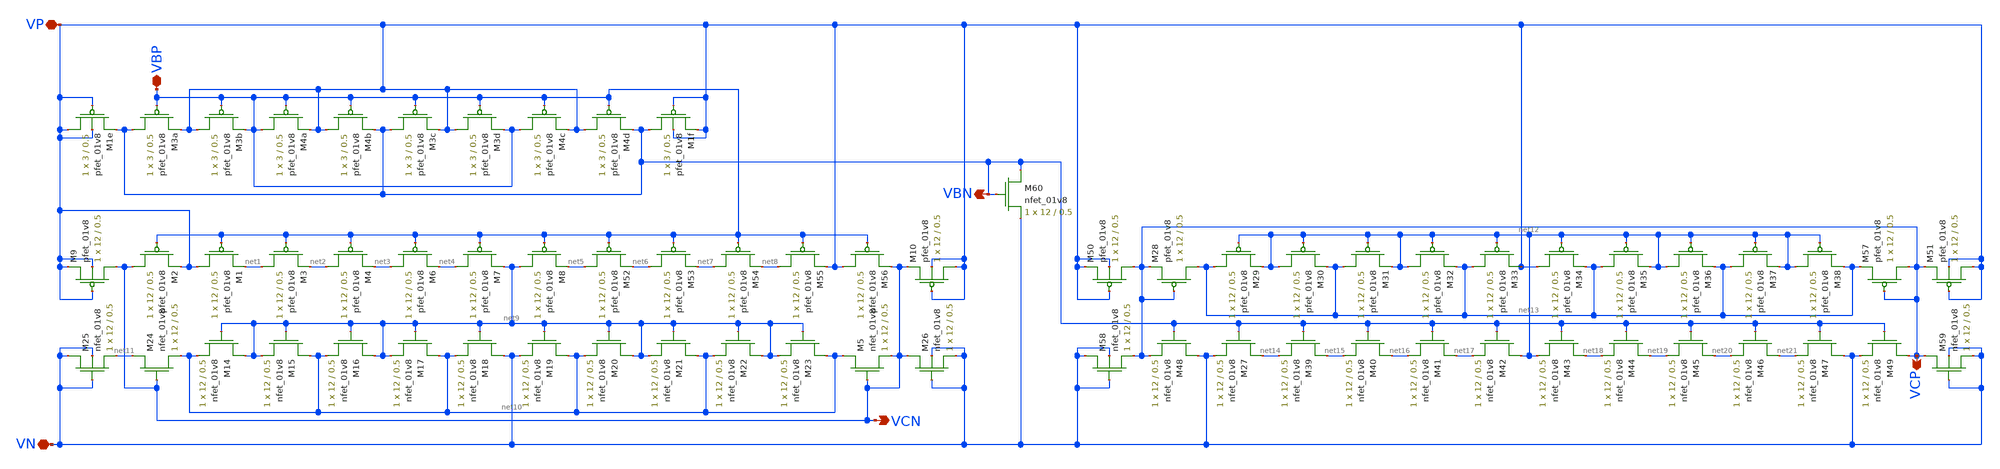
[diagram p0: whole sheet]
** sch_path: mp3/schematics/bias_generator_lds.sch
**.subckt bias_generator_lds VBP VP VN VCN VCP VBN
*.iopin VBP
*.iopin VP
*.iopin VN
*.opin VCN
*.opin VCP
*.opin VBN
XM9 VCN VP VP VP sky130_fd_pr__pfet_01v8 L=0.5 W=12 nf=1 ad='int((nf+1)/2) * W/nf * 0.29' as='int((nf+2)/2) * W/nf * 0.29'
+ pd='2*int((nf+1)/2) * (W/nf + 0.29)' ps='2*int((nf+2)/2) * (W/nf + 0.29)' nrd='0.29 / W' nrs='0.29 / W'
+ sa=0 sb=0 sd=0 mult=1 m=1
XM24 net11 VCN net10 GND sky130_fd_pr__nfet_01v8 L=0.5 W=12 nf=1 ad='int((nf+1)/2) * W/nf * 0.29' as='int((nf+2)/2) * W/nf * 0.29'
+ pd='2*int((nf+1)/2) * (W/nf + 0.29)' ps='2*int((nf+2)/2) * (W/nf + 0.29)' nrd='0.29 / W' nrs='0.29 / W'
+ sa=0 sb=0 sd=0 mult=1 m=1
XM2 VCN VBP VP VDD sky130_fd_pr__pfet_01v8 L=0.5 W=12 nf=1 ad='int((nf+1)/2) * W/nf * 0.29' as='int((nf+2)/2) * W/nf * 0.29'
+ pd='2*int((nf+1)/2) * (W/nf + 0.29)' ps='2*int((nf+2)/2) * (W/nf + 0.29)' nrd='0.29 / W' nrs='0.29 / W'
+ sa=0 sb=0 sd=0 mult=1 m=1
XM1 VP VBP net1 VDD sky130_fd_pr__pfet_01v8 L=0.5 W=12 nf=1 ad='int((nf+1)/2) * W/nf * 0.29' as='int((nf+2)/2) * W/nf * 0.29'
+ pd='2*int((nf+1)/2) * (W/nf + 0.29)' ps='2*int((nf+2)/2) * (W/nf + 0.29)' nrd='0.29 / W' nrs='0.29 / W'
+ sa=0 sb=0 sd=0 mult=1 m=1
XM3 net1 VBP net2 VDD sky130_fd_pr__pfet_01v8 L=0.5 W=12 nf=1 ad='int((nf+1)/2) * W/nf * 0.29' as='int((nf+2)/2) * W/nf * 0.29'
+ pd='2*int((nf+1)/2) * (W/nf + 0.29)' ps='2*int((nf+2)/2) * (W/nf + 0.29)' nrd='0.29 / W' nrs='0.29 / W'
+ sa=0 sb=0 sd=0 mult=1 m=1
XM4 net2 VBP net3 VDD sky130_fd_pr__pfet_01v8 L=0.5 W=12 nf=1 ad='int((nf+1)/2) * W/nf * 0.29' as='int((nf+2)/2) * W/nf * 0.29'
+ pd='2*int((nf+1)/2) * (W/nf + 0.29)' ps='2*int((nf+2)/2) * (W/nf + 0.29)' nrd='0.29 / W' nrs='0.29 / W'
+ sa=0 sb=0 sd=0 mult=1 m=1
XM6 net3 VBP net4 VDD sky130_fd_pr__pfet_01v8 L=0.5 W=12 nf=1 ad='int((nf+1)/2) * W/nf * 0.29' as='int((nf+2)/2) * W/nf * 0.29'
+ pd='2*int((nf+1)/2) * (W/nf + 0.29)' ps='2*int((nf+2)/2) * (W/nf + 0.29)' nrd='0.29 / W' nrs='0.29 / W'
+ sa=0 sb=0 sd=0 mult=1 m=1
XM7 net4 VBP net9 VDD sky130_fd_pr__pfet_01v8 L=0.5 W=12 nf=1 ad='int((nf+1)/2) * W/nf * 0.29' as='int((nf+2)/2) * W/nf * 0.29'
+ pd='2*int((nf+1)/2) * (W/nf + 0.29)' ps='2*int((nf+2)/2) * (W/nf + 0.29)' nrd='0.29 / W' nrs='0.29 / W'
+ sa=0 sb=0 sd=0 mult=1 m=1
XM8 net9 VBP net5 VDD sky130_fd_pr__pfet_01v8 L=0.5 W=12 nf=1 ad='int((nf+1)/2) * W/nf * 0.29' as='int((nf+2)/2) * W/nf * 0.29'
+ pd='2*int((nf+1)/2) * (W/nf + 0.29)' ps='2*int((nf+2)/2) * (W/nf + 0.29)' nrd='0.29 / W' nrs='0.29 / W'
+ sa=0 sb=0 sd=0 mult=1 m=1
XM52 net5 VBP net6 VDD sky130_fd_pr__pfet_01v8 L=0.5 W=12 nf=1 ad='int((nf+1)/2) * W/nf * 0.29' as='int((nf+2)/2) * W/nf * 0.29'
+ pd='2*int((nf+1)/2) * (W/nf + 0.29)' ps='2*int((nf+2)/2) * (W/nf + 0.29)' nrd='0.29 / W' nrs='0.29 / W'
+ sa=0 sb=0 sd=0 mult=1 m=1
XM53 net6 VBP net7 VDD sky130_fd_pr__pfet_01v8 L=0.5 W=12 nf=1 ad='int((nf+1)/2) * W/nf * 0.29' as='int((nf+2)/2) * W/nf * 0.29'
+ pd='2*int((nf+1)/2) * (W/nf + 0.29)' ps='2*int((nf+2)/2) * (W/nf + 0.29)' nrd='0.29 / W' nrs='0.29 / W'
+ sa=0 sb=0 sd=0 mult=1 m=1
XM54 net7 VBP net8 VDD sky130_fd_pr__pfet_01v8 L=0.5 W=12 nf=1 ad='int((nf+1)/2) * W/nf * 0.29' as='int((nf+2)/2) * W/nf * 0.29'
+ pd='2*int((nf+1)/2) * (W/nf + 0.29)' ps='2*int((nf+2)/2) * (W/nf + 0.29)' nrd='0.29 / W' nrs='0.29 / W'
+ sa=0 sb=0 sd=0 mult=1 m=1
XM55 net8 VBP VP VDD sky130_fd_pr__pfet_01v8 L=0.5 W=12 nf=1 ad='int((nf+1)/2) * W/nf * 0.29' as='int((nf+2)/2) * W/nf * 0.29'
+ pd='2*int((nf+1)/2) * (W/nf + 0.29)' ps='2*int((nf+2)/2) * (W/nf + 0.29)' nrd='0.29 / W' nrs='0.29 / W'
+ sa=0 sb=0 sd=0 mult=1 m=1
XM56 VP VBP VCN VDD sky130_fd_pr__pfet_01v8 L=0.5 W=12 nf=1 ad='int((nf+1)/2) * W/nf * 0.29' as='int((nf+2)/2) * W/nf * 0.29'
+ pd='2*int((nf+1)/2) * (W/nf + 0.29)' ps='2*int((nf+2)/2) * (W/nf + 0.29)' nrd='0.29 / W' nrs='0.29 / W'
+ sa=0 sb=0 sd=0 mult=1 m=1
XM10 VP VP VCN VP sky130_fd_pr__pfet_01v8 L=0.5 W=12 nf=1 ad='int((nf+1)/2) * W/nf * 0.29' as='int((nf+2)/2) * W/nf * 0.29'
+ pd='2*int((nf+1)/2) * (W/nf + 0.29)' ps='2*int((nf+2)/2) * (W/nf + 0.29)' nrd='0.29 / W' nrs='0.29 / W'
+ sa=0 sb=0 sd=0 mult=1 m=1
XM25 VN VN net11 VN sky130_fd_pr__nfet_01v8 L=0.5 W=12 nf=1 ad='int((nf+1)/2) * W/nf * 0.29' as='int((nf+2)/2) * W/nf * 0.29'
+ pd='2*int((nf+1)/2) * (W/nf + 0.29)' ps='2*int((nf+2)/2) * (W/nf + 0.29)' nrd='0.29 / W' nrs='0.29 / W'
+ sa=0 sb=0 sd=0 mult=1 m=1
XM14 net9 net9 net10 GND sky130_fd_pr__nfet_01v8 L=0.5 W=12 nf=1 ad='int((nf+1)/2) * W/nf * 0.29' as='int((nf+2)/2) * W/nf * 0.29'
+ pd='2*int((nf+1)/2) * (W/nf + 0.29)' ps='2*int((nf+2)/2) * (W/nf + 0.29)' nrd='0.29 / W' nrs='0.29 / W'
+ sa=0 sb=0 sd=0 mult=1 m=1
XM15 net10 net9 net9 GND sky130_fd_pr__nfet_01v8 L=0.5 W=12 nf=1 ad='int((nf+1)/2) * W/nf * 0.29' as='int((nf+2)/2) * W/nf * 0.29'
+ pd='2*int((nf+1)/2) * (W/nf + 0.29)' ps='2*int((nf+2)/2) * (W/nf + 0.29)' nrd='0.29 / W' nrs='0.29 / W'
+ sa=0 sb=0 sd=0 mult=1 m=1
XM16 net9 net9 net10 GND sky130_fd_pr__nfet_01v8 L=0.5 W=12 nf=1 ad='int((nf+1)/2) * W/nf * 0.29' as='int((nf+2)/2) * W/nf * 0.29'
+ pd='2*int((nf+1)/2) * (W/nf + 0.29)' ps='2*int((nf+2)/2) * (W/nf + 0.29)' nrd='0.29 / W' nrs='0.29 / W'
+ sa=0 sb=0 sd=0 mult=1 m=1
XM17 net10 net9 net9 GND sky130_fd_pr__nfet_01v8 L=0.5 W=12 nf=1 ad='int((nf+1)/2) * W/nf * 0.29' as='int((nf+2)/2) * W/nf * 0.29'
+ pd='2*int((nf+1)/2) * (W/nf + 0.29)' ps='2*int((nf+2)/2) * (W/nf + 0.29)' nrd='0.29 / W' nrs='0.29 / W'
+ sa=0 sb=0 sd=0 mult=1 m=1
XM18 VN net9 net10 GND sky130_fd_pr__nfet_01v8 L=0.5 W=12 nf=1 ad='int((nf+1)/2) * W/nf * 0.29' as='int((nf+2)/2) * W/nf * 0.29'
+ pd='2*int((nf+1)/2) * (W/nf + 0.29)' ps='2*int((nf+2)/2) * (W/nf + 0.29)' nrd='0.29 / W' nrs='0.29 / W'
+ sa=0 sb=0 sd=0 mult=1 m=1
XM19 net10 net9 VN GND sky130_fd_pr__nfet_01v8 L=0.5 W=12 nf=1 ad='int((nf+1)/2) * W/nf * 0.29' as='int((nf+2)/2) * W/nf * 0.29'
+ pd='2*int((nf+1)/2) * (W/nf + 0.29)' ps='2*int((nf+2)/2) * (W/nf + 0.29)' nrd='0.29 / W' nrs='0.29 / W'
+ sa=0 sb=0 sd=0 mult=1 m=1
XM20 net9 net9 net10 GND sky130_fd_pr__nfet_01v8 L=0.5 W=12 nf=1 ad='int((nf+1)/2) * W/nf * 0.29' as='int((nf+2)/2) * W/nf * 0.29'
+ pd='2*int((nf+1)/2) * (W/nf + 0.29)' ps='2*int((nf+2)/2) * (W/nf + 0.29)' nrd='0.29 / W' nrs='0.29 / W'
+ sa=0 sb=0 sd=0 mult=1 m=1
XM21 net10 net9 net9 GND sky130_fd_pr__nfet_01v8 L=0.5 W=12 nf=1 ad='int((nf+1)/2) * W/nf * 0.29' as='int((nf+2)/2) * W/nf * 0.29'
+ pd='2*int((nf+1)/2) * (W/nf + 0.29)' ps='2*int((nf+2)/2) * (W/nf + 0.29)' nrd='0.29 / W' nrs='0.29 / W'
+ sa=0 sb=0 sd=0 mult=1 m=1
XM22 net9 net9 net10 GND sky130_fd_pr__nfet_01v8 L=0.5 W=12 nf=1 ad='int((nf+1)/2) * W/nf * 0.29' as='int((nf+2)/2) * W/nf * 0.29'
+ pd='2*int((nf+1)/2) * (W/nf + 0.29)' ps='2*int((nf+2)/2) * (W/nf + 0.29)' nrd='0.29 / W' nrs='0.29 / W'
+ sa=0 sb=0 sd=0 mult=1 m=1
XM23 net10 net9 net9 GND sky130_fd_pr__nfet_01v8 L=0.5 W=12 nf=1 ad='int((nf+1)/2) * W/nf * 0.29' as='int((nf+2)/2) * W/nf * 0.29'
+ pd='2*int((nf+1)/2) * (W/nf + 0.29)' ps='2*int((nf+2)/2) * (W/nf + 0.29)' nrd='0.29 / W' nrs='0.29 / W'
+ sa=0 sb=0 sd=0 mult=1 m=1
XM5 net10 VCN VCN GND sky130_fd_pr__nfet_01v8 L=0.5 W=12 nf=1 ad='int((nf+1)/2) * W/nf * 0.29' as='int((nf+2)/2) * W/nf * 0.29'
+ pd='2*int((nf+1)/2) * (W/nf + 0.29)' ps='2*int((nf+2)/2) * (W/nf + 0.29)' nrd='0.29 / W' nrs='0.29 / W'
+ sa=0 sb=0 sd=0 mult=1 m=1
XM26 VCN VN VN VN sky130_fd_pr__nfet_01v8 L=0.5 W=12 nf=1 ad='int((nf+1)/2) * W/nf * 0.29' as='int((nf+2)/2) * W/nf * 0.29'
+ pd='2*int((nf+1)/2) * (W/nf + 0.29)' ps='2*int((nf+2)/2) * (W/nf + 0.29)' nrd='0.29 / W' nrs='0.29 / W'
+ sa=0 sb=0 sd=0 mult=1 m=1
XM27 net14 VBN VN GND sky130_fd_pr__nfet_01v8 L=0.5 W=12 nf=1 ad='int((nf+1)/2) * W/nf * 0.29' as='int((nf+2)/2) * W/nf * 0.29'
+ pd='2*int((nf+1)/2) * (W/nf + 0.29)' ps='2*int((nf+2)/2) * (W/nf + 0.29)' nrd='0.29 / W' nrs='0.29 / W'
+ sa=0 sb=0 sd=0 mult=1 m=1
XM39 net15 VBN net14 GND sky130_fd_pr__nfet_01v8 L=0.5 W=12 nf=1 ad='int((nf+1)/2) * W/nf * 0.29' as='int((nf+2)/2) * W/nf * 0.29'
+ pd='2*int((nf+1)/2) * (W/nf + 0.29)' ps='2*int((nf+2)/2) * (W/nf + 0.29)' nrd='0.29 / W' nrs='0.29 / W'
+ sa=0 sb=0 sd=0 mult=1 m=1
XM40 net16 VBN net15 GND sky130_fd_pr__nfet_01v8 L=0.5 W=12 nf=1 ad='int((nf+1)/2) * W/nf * 0.29' as='int((nf+2)/2) * W/nf * 0.29'
+ pd='2*int((nf+1)/2) * (W/nf + 0.29)' ps='2*int((nf+2)/2) * (W/nf + 0.29)' nrd='0.29 / W' nrs='0.29 / W'
+ sa=0 sb=0 sd=0 mult=1 m=1
XM41 net17 VBN net16 GND sky130_fd_pr__nfet_01v8 L=0.5 W=12 nf=1 ad='int((nf+1)/2) * W/nf * 0.29' as='int((nf+2)/2) * W/nf * 0.29'
+ pd='2*int((nf+1)/2) * (W/nf + 0.29)' ps='2*int((nf+2)/2) * (W/nf + 0.29)' nrd='0.29 / W' nrs='0.29 / W'
+ sa=0 sb=0 sd=0 mult=1 m=1
XM42 net12 VBN net17 GND sky130_fd_pr__nfet_01v8 L=0.5 W=12 nf=1 ad='int((nf+1)/2) * W/nf * 0.29' as='int((nf+2)/2) * W/nf * 0.29'
+ pd='2*int((nf+1)/2) * (W/nf + 0.29)' ps='2*int((nf+2)/2) * (W/nf + 0.29)' nrd='0.29 / W' nrs='0.29 / W'
+ sa=0 sb=0 sd=0 mult=1 m=1
XM43 net18 VBN net12 GND sky130_fd_pr__nfet_01v8 L=0.5 W=12 nf=1 ad='int((nf+1)/2) * W/nf * 0.29' as='int((nf+2)/2) * W/nf * 0.29'
+ pd='2*int((nf+1)/2) * (W/nf + 0.29)' ps='2*int((nf+2)/2) * (W/nf + 0.29)' nrd='0.29 / W' nrs='0.29 / W'
+ sa=0 sb=0 sd=0 mult=1 m=1
XM44 net19 VBN net18 GND sky130_fd_pr__nfet_01v8 L=0.5 W=12 nf=1 ad='int((nf+1)/2) * W/nf * 0.29' as='int((nf+2)/2) * W/nf * 0.29'
+ pd='2*int((nf+1)/2) * (W/nf + 0.29)' ps='2*int((nf+2)/2) * (W/nf + 0.29)' nrd='0.29 / W' nrs='0.29 / W'
+ sa=0 sb=0 sd=0 mult=1 m=1
XM45 net20 VBN net19 GND sky130_fd_pr__nfet_01v8 L=0.5 W=12 nf=1 ad='int((nf+1)/2) * W/nf * 0.29' as='int((nf+2)/2) * W/nf * 0.29'
+ pd='2*int((nf+1)/2) * (W/nf + 0.29)' ps='2*int((nf+2)/2) * (W/nf + 0.29)' nrd='0.29 / W' nrs='0.29 / W'
+ sa=0 sb=0 sd=0 mult=1 m=1
XM46 net21 VBN net20 GND sky130_fd_pr__nfet_01v8 L=0.5 W=12 nf=1 ad='int((nf+1)/2) * W/nf * 0.29' as='int((nf+2)/2) * W/nf * 0.29'
+ pd='2*int((nf+1)/2) * (W/nf + 0.29)' ps='2*int((nf+2)/2) * (W/nf + 0.29)' nrd='0.29 / W' nrs='0.29 / W'
+ sa=0 sb=0 sd=0 mult=1 m=1
XM47 VN VBN net21 GND sky130_fd_pr__nfet_01v8 L=0.5 W=12 nf=1 ad='int((nf+1)/2) * W/nf * 0.29' as='int((nf+2)/2) * W/nf * 0.29'
+ pd='2*int((nf+1)/2) * (W/nf + 0.29)' ps='2*int((nf+2)/2) * (W/nf + 0.29)' nrd='0.29 / W' nrs='0.29 / W'
+ sa=0 sb=0 sd=0 mult=1 m=1
XM48 VN VBN VCP GND sky130_fd_pr__nfet_01v8 L=0.5 W=12 nf=1 ad='int((nf+1)/2) * W/nf * 0.29' as='int((nf+2)/2) * W/nf * 0.29'
+ pd='2*int((nf+1)/2) * (W/nf + 0.29)' ps='2*int((nf+2)/2) * (W/nf + 0.29)' nrd='0.29 / W' nrs='0.29 / W'
+ sa=0 sb=0 sd=0 mult=1 m=1
XM49 VCP VBN VN GND sky130_fd_pr__nfet_01v8 L=0.5 W=12 nf=1 ad='int((nf+1)/2) * W/nf * 0.29' as='int((nf+2)/2) * W/nf * 0.29'
+ pd='2*int((nf+1)/2) * (W/nf + 0.29)' ps='2*int((nf+2)/2) * (W/nf + 0.29)' nrd='0.29 / W' nrs='0.29 / W'
+ sa=0 sb=0 sd=0 mult=1 m=1
XM29 net13 net12 net12 VDD sky130_fd_pr__pfet_01v8 L=0.5 W=12 nf=1 ad='int((nf+1)/2) * W/nf * 0.29' as='int((nf+2)/2) * W/nf * 0.29'
+ pd='2*int((nf+1)/2) * (W/nf + 0.29)' ps='2*int((nf+2)/2) * (W/nf + 0.29)' nrd='0.29 / W' nrs='0.29 / W'
+ sa=0 sb=0 sd=0 mult=1 m=1
XM30 net12 net12 net13 VDD sky130_fd_pr__pfet_01v8 L=0.5 W=12 nf=1 ad='int((nf+1)/2) * W/nf * 0.29' as='int((nf+2)/2) * W/nf * 0.29'
+ pd='2*int((nf+1)/2) * (W/nf + 0.29)' ps='2*int((nf+2)/2) * (W/nf + 0.29)' nrd='0.29 / W' nrs='0.29 / W'
+ sa=0 sb=0 sd=0 mult=1 m=1
XM31 net13 net12 net12 VDD sky130_fd_pr__pfet_01v8 L=0.5 W=12 nf=1 ad='int((nf+1)/2) * W/nf * 0.29' as='int((nf+2)/2) * W/nf * 0.29'
+ pd='2*int((nf+1)/2) * (W/nf + 0.29)' ps='2*int((nf+2)/2) * (W/nf + 0.29)' nrd='0.29 / W' nrs='0.29 / W'
+ sa=0 sb=0 sd=0 mult=1 m=1
XM32 net12 net12 net13 VDD sky130_fd_pr__pfet_01v8 L=0.5 W=12 nf=1 ad='int((nf+1)/2) * W/nf * 0.29' as='int((nf+2)/2) * W/nf * 0.29'
+ pd='2*int((nf+1)/2) * (W/nf + 0.29)' ps='2*int((nf+2)/2) * (W/nf + 0.29)' nrd='0.29 / W' nrs='0.29 / W'
+ sa=0 sb=0 sd=0 mult=1 m=1
XM33 net13 net12 VP VDD sky130_fd_pr__pfet_01v8 L=0.5 W=12 nf=1 ad='int((nf+1)/2) * W/nf * 0.29' as='int((nf+2)/2) * W/nf * 0.29'
+ pd='2*int((nf+1)/2) * (W/nf + 0.29)' ps='2*int((nf+2)/2) * (W/nf + 0.29)' nrd='0.29 / W' nrs='0.29 / W'
+ sa=0 sb=0 sd=0 mult=1 m=1
XM34 VP net12 net13 VDD sky130_fd_pr__pfet_01v8 L=0.5 W=12 nf=1 ad='int((nf+1)/2) * W/nf * 0.29' as='int((nf+2)/2) * W/nf * 0.29'
+ pd='2*int((nf+1)/2) * (W/nf + 0.29)' ps='2*int((nf+2)/2) * (W/nf + 0.29)' nrd='0.29 / W' nrs='0.29 / W'
+ sa=0 sb=0 sd=0 mult=1 m=1
XM35 net13 net12 net12 VDD sky130_fd_pr__pfet_01v8 L=0.5 W=12 nf=1 ad='int((nf+1)/2) * W/nf * 0.29' as='int((nf+2)/2) * W/nf * 0.29'
+ pd='2*int((nf+1)/2) * (W/nf + 0.29)' ps='2*int((nf+2)/2) * (W/nf + 0.29)' nrd='0.29 / W' nrs='0.29 / W'
+ sa=0 sb=0 sd=0 mult=1 m=1
XM36 net12 net12 net13 VDD sky130_fd_pr__pfet_01v8 L=0.5 W=12 nf=1 ad='int((nf+1)/2) * W/nf * 0.29' as='int((nf+2)/2) * W/nf * 0.29'
+ pd='2*int((nf+1)/2) * (W/nf + 0.29)' ps='2*int((nf+2)/2) * (W/nf + 0.29)' nrd='0.29 / W' nrs='0.29 / W'
+ sa=0 sb=0 sd=0 mult=1 m=1
XM37 net13 net12 net12 VDD sky130_fd_pr__pfet_01v8 L=0.5 W=12 nf=1 ad='int((nf+1)/2) * W/nf * 0.29' as='int((nf+2)/2) * W/nf * 0.29'
+ pd='2*int((nf+1)/2) * (W/nf + 0.29)' ps='2*int((nf+2)/2) * (W/nf + 0.29)' nrd='0.29 / W' nrs='0.29 / W'
+ sa=0 sb=0 sd=0 mult=1 m=1
XM38 net12 net12 net13 VDD sky130_fd_pr__pfet_01v8 L=0.5 W=12 nf=1 ad='int((nf+1)/2) * W/nf * 0.29' as='int((nf+2)/2) * W/nf * 0.29'
+ pd='2*int((nf+1)/2) * (W/nf + 0.29)' ps='2*int((nf+2)/2) * (W/nf + 0.29)' nrd='0.29 / W' nrs='0.29 / W'
+ sa=0 sb=0 sd=0 mult=1 m=1
XM57 VCP VCP net13 VDD sky130_fd_pr__pfet_01v8 L=0.5 W=12 nf=1 ad='int((nf+1)/2) * W/nf * 0.29' as='int((nf+2)/2) * W/nf * 0.29'
+ pd='2*int((nf+1)/2) * (W/nf + 0.29)' ps='2*int((nf+2)/2) * (W/nf + 0.29)' nrd='0.29 / W' nrs='0.29 / W'
+ sa=0 sb=0 sd=0 mult=1 m=1
XM28 net13 VCP VCP VDD sky130_fd_pr__pfet_01v8 L=0.5 W=12 nf=1 ad='int((nf+1)/2) * W/nf * 0.29' as='int((nf+2)/2) * W/nf * 0.29'
+ pd='2*int((nf+1)/2) * (W/nf + 0.29)' ps='2*int((nf+2)/2) * (W/nf + 0.29)' nrd='0.29 / W' nrs='0.29 / W'
+ sa=0 sb=0 sd=0 mult=1 m=1
XM50 VCP VP VP VP sky130_fd_pr__pfet_01v8 L=0.5 W=12 nf=1 ad='int((nf+1)/2) * W/nf * 0.29' as='int((nf+2)/2) * W/nf * 0.29'
+ pd='2*int((nf+1)/2) * (W/nf + 0.29)' ps='2*int((nf+2)/2) * (W/nf + 0.29)' nrd='0.29 / W' nrs='0.29 / W'
+ sa=0 sb=0 sd=0 mult=1 m=1
XM51 VP VP VCP VP sky130_fd_pr__pfet_01v8 L=0.5 W=12 nf=1 ad='int((nf+1)/2) * W/nf * 0.29' as='int((nf+2)/2) * W/nf * 0.29'
+ pd='2*int((nf+1)/2) * (W/nf + 0.29)' ps='2*int((nf+2)/2) * (W/nf + 0.29)' nrd='0.29 / W' nrs='0.29 / W'
+ sa=0 sb=0 sd=0 mult=1 m=1
XM58 VN VN VCP VN sky130_fd_pr__nfet_01v8 L=0.5 W=12 nf=1 ad='int((nf+1)/2) * W/nf * 0.29' as='int((nf+2)/2) * W/nf * 0.29'
+ pd='2*int((nf+1)/2) * (W/nf + 0.29)' ps='2*int((nf+2)/2) * (W/nf + 0.29)' nrd='0.29 / W' nrs='0.29 / W'
+ sa=0 sb=0 sd=0 mult=1 m=1
XM59 VCP VN VN VN sky130_fd_pr__nfet_01v8 L=0.5 W=12 nf=1 ad='int((nf+1)/2) * W/nf * 0.29' as='int((nf+2)/2) * W/nf * 0.29'
+ pd='2*int((nf+1)/2) * (W/nf + 0.29)' ps='2*int((nf+2)/2) * (W/nf + 0.29)' nrd='0.29 / W' nrs='0.29 / W'
+ sa=0 sb=0 sd=0 mult=1 m=1
XM3b VP VBP VBP VDD sky130_fd_pr__pfet_01v8 L=0.5 W=3 nf=1 ad='int((nf+1)/2) * W/nf * 0.29' as='int((nf+2)/2) * W/nf * 0.29'
+ pd='2*int((nf+1)/2) * (W/nf + 0.29)' ps='2*int((nf+2)/2) * (W/nf + 0.29)' nrd='0.29 / W' nrs='0.29 / W'
+ sa=0 sb=0 sd=0 mult=1 m=1
XM3a VBN VBP VP VDD sky130_fd_pr__pfet_01v8 L=0.5 W=3 nf=1 ad='int((nf+1)/2) * W/nf * 0.29' as='int((nf+2)/2) * W/nf * 0.29'
+ pd='2*int((nf+1)/2) * (W/nf + 0.29)' ps='2*int((nf+2)/2) * (W/nf + 0.29)' nrd='0.29 / W' nrs='0.29 / W'
+ sa=0 sb=0 sd=0 mult=1 m=1
XM4a VBP VBP VP VDD sky130_fd_pr__pfet_01v8 L=0.5 W=3 nf=1 ad='int((nf+1)/2) * W/nf * 0.29' as='int((nf+2)/2) * W/nf * 0.29'
+ pd='2*int((nf+1)/2) * (W/nf + 0.29)' ps='2*int((nf+2)/2) * (W/nf + 0.29)' nrd='0.29 / W' nrs='0.29 / W'
+ sa=0 sb=0 sd=0 mult=1 m=1
XM4b VP VBP VBN VDD sky130_fd_pr__pfet_01v8 L=0.5 W=3 nf=1 ad='int((nf+1)/2) * W/nf * 0.29' as='int((nf+2)/2) * W/nf * 0.29'
+ pd='2*int((nf+1)/2) * (W/nf + 0.29)' ps='2*int((nf+2)/2) * (W/nf + 0.29)' nrd='0.29 / W' nrs='0.29 / W'
+ sa=0 sb=0 sd=0 mult=1 m=1
XM3c VBN VBP VP VDD sky130_fd_pr__pfet_01v8 L=0.5 W=3 nf=1 ad='int((nf+1)/2) * W/nf * 0.29' as='int((nf+2)/2) * W/nf * 0.29'
+ pd='2*int((nf+1)/2) * (W/nf + 0.29)' ps='2*int((nf+2)/2) * (W/nf + 0.29)' nrd='0.29 / W' nrs='0.29 / W'
+ sa=0 sb=0 sd=0 mult=1 m=1
XM3d VP VBP VBP VDD sky130_fd_pr__pfet_01v8 L=0.5 W=3 nf=1 ad='int((nf+1)/2) * W/nf * 0.29' as='int((nf+2)/2) * W/nf * 0.29'
+ pd='2*int((nf+1)/2) * (W/nf + 0.29)' ps='2*int((nf+2)/2) * (W/nf + 0.29)' nrd='0.29 / W' nrs='0.29 / W'
+ sa=0 sb=0 sd=0 mult=1 m=1
XM4c VBP VBP VP VDD sky130_fd_pr__pfet_01v8 L=0.5 W=3 nf=1 ad='int((nf+1)/2) * W/nf * 0.29' as='int((nf+2)/2) * W/nf * 0.29'
+ pd='2*int((nf+1)/2) * (W/nf + 0.29)' ps='2*int((nf+2)/2) * (W/nf + 0.29)' nrd='0.29 / W' nrs='0.29 / W'
+ sa=0 sb=0 sd=0 mult=1 m=1
XM1e VP VP VBN VP sky130_fd_pr__pfet_01v8 L=0.5 W=3 nf=1 ad='int((nf+1)/2) * W/nf * 0.29' as='int((nf+2)/2) * W/nf * 0.29'
+ pd='2*int((nf+1)/2) * (W/nf + 0.29)' ps='2*int((nf+2)/2) * (W/nf + 0.29)' nrd='0.29 / W' nrs='0.29 / W'
+ sa=0 sb=0 sd=0 mult=1 m=1
XM1f VBN VP VP VP sky130_fd_pr__pfet_01v8 L=0.5 W=3 nf=1 ad='int((nf+1)/2) * W/nf * 0.29' as='int((nf+2)/2) * W/nf * 0.29'
+ pd='2*int((nf+1)/2) * (W/nf + 0.29)' ps='2*int((nf+2)/2) * (W/nf + 0.29)' nrd='0.29 / W' nrs='0.29 / W'
+ sa=0 sb=0 sd=0 mult=1 m=1
XM4d VP VBP VBN VDD sky130_fd_pr__pfet_01v8 L=0.5 W=3 nf=1 ad='int((nf+1)/2) * W/nf * 0.29' as='int((nf+2)/2) * W/nf * 0.29'
+ pd='2*int((nf+1)/2) * (W/nf + 0.29)' ps='2*int((nf+2)/2) * (W/nf + 0.29)' nrd='0.29 / W' nrs='0.29 / W'
+ sa=0 sb=0 sd=0 mult=1 m=1
XM60 VBN VBN VN GND sky130_fd_pr__nfet_01v8 L=0.5 W=12 nf=1 ad='int((nf+1)/2) * W/nf * 0.29' as='int((nf+2)/2) * W/nf * 0.29'
+ pd='2*int((nf+1)/2) * (W/nf + 0.29)' ps='2*int((nf+2)/2) * (W/nf + 0.29)' nrd='0.29 / W' nrs='0.29 / W'
+ sa=0 sb=0 sd=0 mult=1 m=1
**.ends
.end
